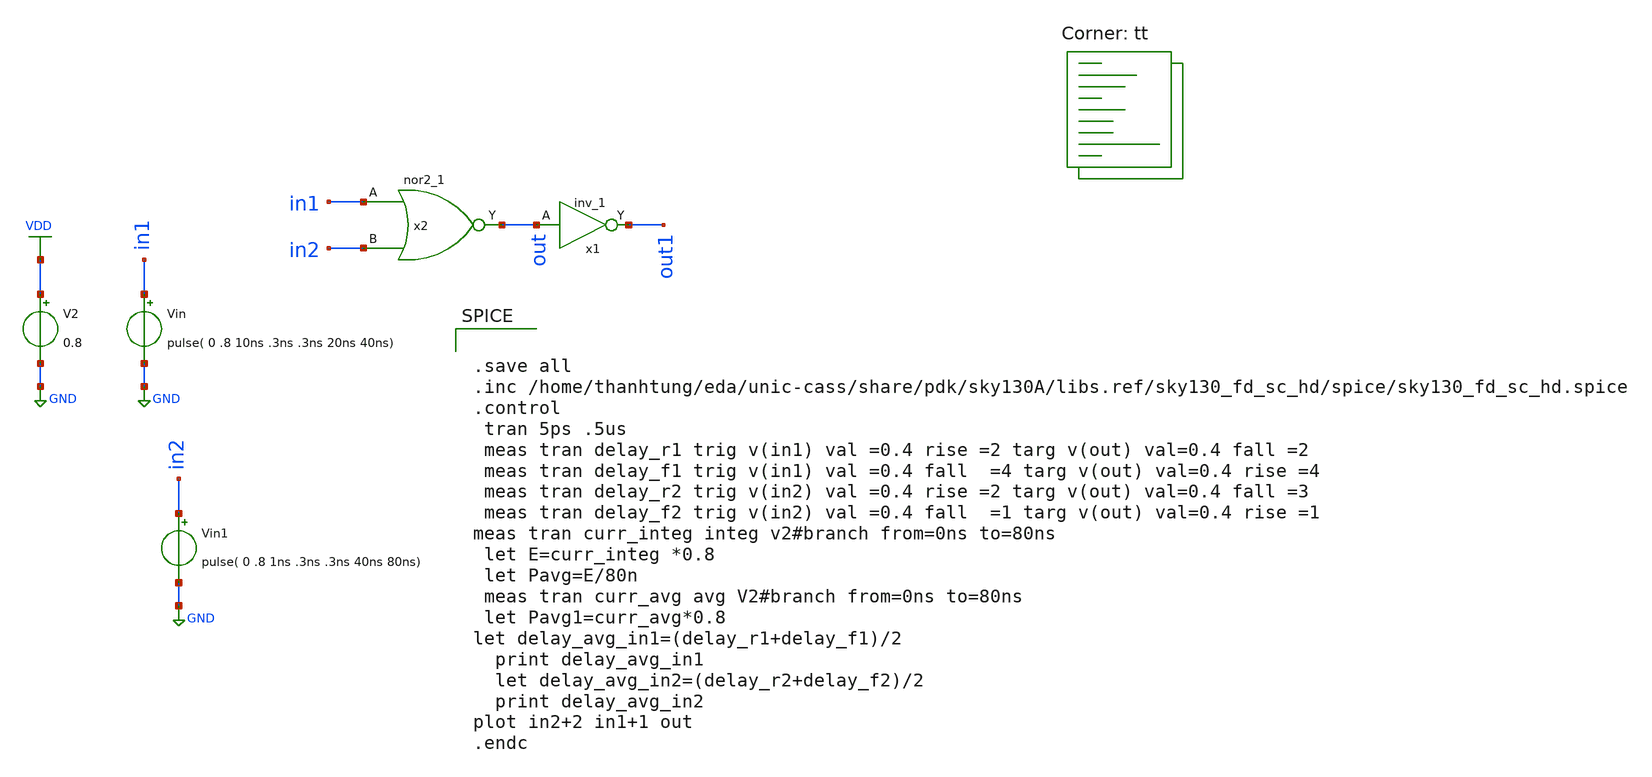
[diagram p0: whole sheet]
** sch_path: d_nor2_fan.sch
**.subckt d_nor2_fan
V2 VDD GND 0.8
Vin in1 GND pulse( 0 .8 10ns .3ns .3ns 20ns 40ns)
Vin1 in2 GND pulse( 0 .8 1ns .3ns .3ns 40ns 80ns)
x2 in1 in2 GND GND VDD VDD out sky130_fd_sc_hd__nor2_1
x1 out GND GND VDD VDD out1 sky130_fd_sc_hd__inv_1
**** begin user architecture code


.save all
.inc /home/thanhtung/eda/unic-cass/share/pdk/sky130A/libs.ref/sky130_fd_sc_hd/spice/sky130_fd_sc_hd.spice
.control
 tran 5ps .5us
 meas tran delay_r1 trig v(in1) val =0.4 rise =2 targ v(out) val=0.4 fall =2
 meas tran delay_f1 trig v(in1) val =0.4 fall  =4 targ v(out) val=0.4 rise =4
 meas tran delay_r2 trig v(in2) val =0.4 rise =2 targ v(out) val=0.4 fall =3
 meas tran delay_f2 trig v(in2) val =0.4 fall  =1 targ v(out) val=0.4 rise =1
meas tran curr_integ integ v2#branch from=0ns to=80ns
 let E=curr_integ *0.8
 let Pavg=E/80n
 meas tran curr_avg avg V2#branch from=0ns to=80ns
 let Pavg1=curr_avg*0.8
let delay_avg_in1=(delay_r1+delay_f1)/2
  print delay_avg_in1
  let delay_avg_in2=(delay_r2+delay_f2)/2
  print delay_avg_in2
plot in2+2 in1+1 out
.endc


.lib $::SKYWATER_MODELS/sky130.lib.spice tt
**** end user architecture code
**.ends
.GLOBAL GND
.GLOBAL VDD
.end
